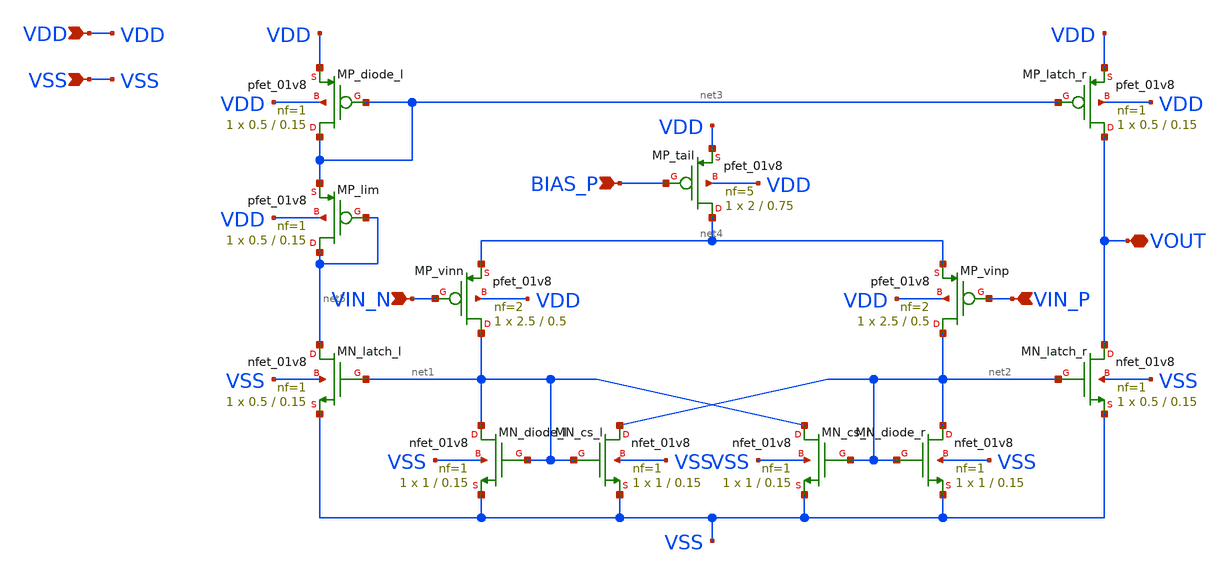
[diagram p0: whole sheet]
** sch_path: schem/symbol_repo/sym_comp_p.sch
**.subckt sym_comp_p VDD VSS BIAS_P VIN_N VIN_P VOUT
*.ipin VDD
*.ipin VSS
*.ipin BIAS_P
*.ipin VIN_N
*.ipin VIN_P
*.iopin VOUT
XMN_cs_l net2 net1 VSS VSS sky130_fd_pr__nfet_01v8 L=0.15 W=1 nf=1 ad='int((1 + 1)/2) * 1 / 1 * 0.29'
+ as='int((1 + 2)/2) * 1 / 1 * 0.29' pd='2*int((1 + 1)/2) * (1 / 1 + 0.29)' ps='2*int((1 + 2)/2) * (1 / 1 + 0.29)'
+ nrd='0.29 / 1 ' nrs='0.29 / 1 ' sa=0 sb=0 sd=0 mult=1 m=1
XMP_tail net4 BIAS_P VDD VDD sky130_fd_pr__pfet_01v8 L=0.75 W=2 nf=5 ad='int((5 + 1)/2) * 2 / 5 * 0.29'
+ as='int((5 + 2)/2) * 2 / 5 * 0.29' pd='2*int((5 + 1)/2) * (2 / 5 + 0.29)' ps='2*int((5 + 2)/2) * (2 / 5 + 0.29)'
+ nrd='0.29 / 2 ' nrs='0.29 / 2 ' sa=0 sb=0 sd=0 mult=1 m=1
XMP_vinn net1 VIN_N net4 VDD sky130_fd_pr__pfet_01v8 L=0.5 W=2.5 nf=2 ad='int((2 + 1)/2) * 2.5 / 2 * 0.29'
+ as='int((2 + 2)/2) * 2.5 / 2 * 0.29' pd='2*int((2 + 1)/2) * (2.5 / 2 + 0.29)' ps='2*int((2 + 2)/2) * (2.5 / 2 + 0.29)'
+ nrd='0.29 / 2.5 ' nrs='0.29 / 2.5 ' sa=0 sb=0 sd=0 mult=1 m=1
XMP_vinp net2 VIN_P net4 VDD sky130_fd_pr__pfet_01v8 L=0.5 W=2.5 nf=2 ad='int((2 + 1)/2) * 2.5 / 2 * 0.29'
+ as='int((2 + 2)/2) * 2.5 / 2 * 0.29' pd='2*int((2 + 1)/2) * (2.5 / 2 + 0.29)' ps='2*int((2 + 2)/2) * (2.5 / 2 + 0.29)'
+ nrd='0.29 / 2.5 ' nrs='0.29 / 2.5 ' sa=0 sb=0 sd=0 mult=1 m=1
XMN_diode_l net1 net1 VSS VSS sky130_fd_pr__nfet_01v8 L=0.15 W=1 nf=1 ad='int((1 + 1)/2) * 1 / 1 * 0.29'
+ as='int((1 + 2)/2) * 1 / 1 * 0.29' pd='2*int((1 + 1)/2) * (1 / 1 + 0.29)' ps='2*int((1 + 2)/2) * (1 / 1 + 0.29)'
+ nrd='0.29 / 1 ' nrs='0.29 / 1 ' sa=0 sb=0 sd=0 mult=1 m=1
XMN_diode_r net2 net2 VSS VSS sky130_fd_pr__nfet_01v8 L=0.15 W=1 nf=1 ad='int((1 + 1)/2) * 1 / 1 * 0.29'
+ as='int((1 + 2)/2) * 1 / 1 * 0.29' pd='2*int((1 + 1)/2) * (1 / 1 + 0.29)' ps='2*int((1 + 2)/2) * (1 / 1 + 0.29)'
+ nrd='0.29 / 1 ' nrs='0.29 / 1 ' sa=0 sb=0 sd=0 mult=1 m=1
XMN_cs_r net1 net2 VSS VSS sky130_fd_pr__nfet_01v8 L=0.15 W=1 nf=1 ad='int((1 + 1)/2) * 1 / 1 * 0.29'
+ as='int((1 + 2)/2) * 1 / 1 * 0.29' pd='2*int((1 + 1)/2) * (1 / 1 + 0.29)' ps='2*int((1 + 2)/2) * (1 / 1 + 0.29)'
+ nrd='0.29 / 1 ' nrs='0.29 / 1 ' sa=0 sb=0 sd=0 mult=1 m=1
XMN_latch_l net5 net1 VSS VSS sky130_fd_pr__nfet_01v8 L=0.15 W=0.5 nf=1 ad='int((1 + 1)/2) * 0.5 / 1 * 0.29'
+ as='int((1 + 2)/2) * 0.5 / 1 * 0.29' pd='2*int((1 + 1)/2) * (0.5 / 1 + 0.29)' ps='2*int((1 + 2)/2) * (0.5 / 1 + 0.29)'
+ nrd='0.29 / 0.5 ' nrs='0.29 / 0.5 ' sa=0 sb=0 sd=0 mult=1 m=1
XMN_latch_r VOUT net2 VSS VSS sky130_fd_pr__nfet_01v8 L=0.15 W=0.5 nf=1 ad='int((1 + 1)/2) * 0.5 / 1 * 0.29'
+ as='int((1 + 2)/2) * 0.5 / 1 * 0.29' pd='2*int((1 + 1)/2) * (0.5 / 1 + 0.29)' ps='2*int((1 + 2)/2) * (0.5 / 1 + 0.29)'
+ nrd='0.29 / 0.5 ' nrs='0.29 / 0.5 ' sa=0 sb=0 sd=0 mult=1 m=1
XMP_diode_l net3 net3 VDD VDD sky130_fd_pr__pfet_01v8 L=0.15 W=0.5 nf=1 ad='int((1 + 1)/2) * 0.5 / 1 * 0.29'
+ as='int((1 + 2)/2) * 0.5 / 1 * 0.29' pd='2*int((1 + 1)/2) * (0.5 / 1 + 0.29)' ps='2*int((1 + 2)/2) * (0.5 / 1 + 0.29)'
+ nrd='0.29 / 0.5 ' nrs='0.29 / 0.5 ' sa=0 sb=0 sd=0 mult=1 m=1
XMP_latch_r VOUT net3 VDD VDD sky130_fd_pr__pfet_01v8 L=0.15 W=0.5 nf=1 ad='int((1 + 1)/2) * 0.5 / 1 * 0.29'
+ as='int((1 + 2)/2) * 0.5 / 1 * 0.29' pd='2*int((1 + 1)/2) * (0.5 / 1 + 0.29)' ps='2*int((1 + 2)/2) * (0.5 / 1 + 0.29)'
+ nrd='0.29 / 0.5 ' nrs='0.29 / 0.5 ' sa=0 sb=0 sd=0 mult=1 m=1
XMP_lim net5 net5 net3 VDD sky130_fd_pr__pfet_01v8 L=0.15 W=0.5 nf=1 ad='int((1 + 1)/2) * 0.5 / 1 * 0.29'
+ as='int((1 + 2)/2) * 0.5 / 1 * 0.29' pd='2*int((1 + 1)/2) * (0.5 / 1 + 0.29)' ps='2*int((1 + 2)/2) * (0.5 / 1 + 0.29)'
+ nrd='0.29 / 0.5 ' nrs='0.29 / 0.5 ' sa=0 sb=0 sd=0 mult=1 m=1
**.ends
.end
